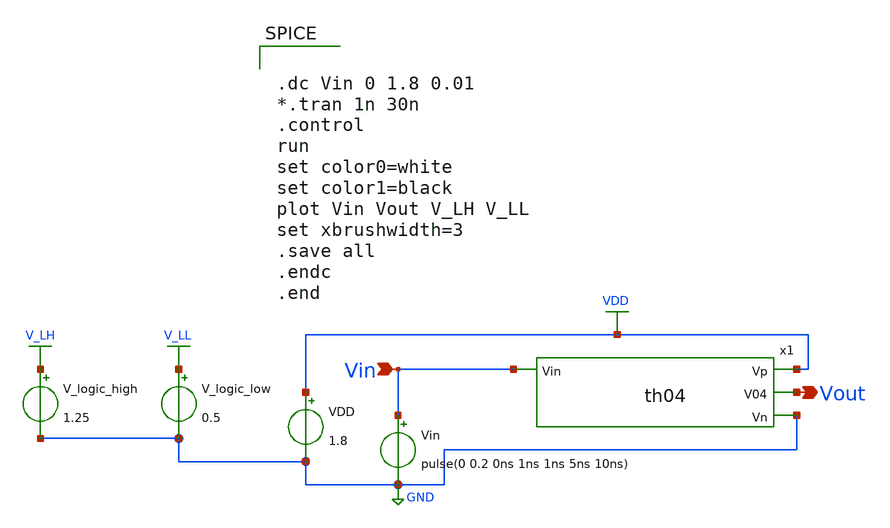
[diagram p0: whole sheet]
** sch_path: xschem/Vth_sch/Pre_layout/th04.sch
**.subckt th04 Vin Vout
*.ipin Vin
*.opin Vout
VDD VDD GND 1.8
Vin Vin GND pulse(0 0.2 0ns 1ns 1ns 5ns 10ns)
V_logic_high V_LH GND 1.25
V_logic_low V_LL GND 0.5
x1 VDD Vout Vin GND th04
**** begin user architecture code


.lib /usr/local/share/pdk/sky130A/libs.tech/ngspice/sky130.lib.spice tt

.save all





.dc Vin 0 1.8 0.01
*.tran 1n 30n
.control
run
set color0=white
set color1=black
plot Vin Vout V_LH V_LL
set xbrushwidth=3
.save all
.endc
.end


**** end user architecture code
**.ends

* expanding   symbol:  /home/exotic/Desktop/ASIC_ADC/xschem/Vth_sch/Symbol/th04.sym # of pins=4
** sym_path: xschem/Vth_sch/Symbol/th04.sym
** sch_path: xschem/Vth_sch/Symbol/th04.sch
.subckt th04 Vp V04 Vin Vn
*.opin Vn
*.opin Vp
*.ipin Vin
*.opin V04
XM3 V04 net1 Vp Vp sky130_fd_pr__pfet_01v8 L=0.220 W=0.42 nf=1 ad='int((nf+1)/2) * W/nf * 0.29' as='int((nf+2)/2) * W/nf * 0.29'
+ pd='2*int((nf+1)/2) * (W/nf + 0.29)' ps='2*int((nf+2)/2) * (W/nf + 0.29)' nrd='0.29 / W' nrs='0.29 / W'
+ sa=0 sb=0 sd=0 mult=1 m=1
XM4 V04 net1 Vn Vn sky130_fd_pr__nfet_01v8 L=0.193 W=0.36 nf=1 ad='int((nf+1)/2) * W/nf * 0.29' as='int((nf+2)/2) * W/nf * 0.29'
+ pd='2*int((nf+1)/2) * (W/nf + 0.29)' ps='2*int((nf+2)/2) * (W/nf + 0.29)' nrd='0.29 / W' nrs='0.29 / W'
+ sa=0 sb=0 sd=0 mult=1 m=1
XM1 net1 Vin net2 Vp sky130_fd_pr__pfet_01v8 L=0.193 W=0.42 nf=1 ad='int((nf+1)/2) * W/nf * 0.29' as='int((nf+2)/2) * W/nf * 0.29'
+ pd='2*int((nf+1)/2) * (W/nf + 0.29)' ps='2*int((nf+2)/2) * (W/nf + 0.29)' nrd='0.29 / W' nrs='0.29 / W'
+ sa=0 sb=0 sd=0 mult=1 m=1
XM0 net1 Vin Vn Vn sky130_fd_pr__nfet_01v8 L=0.220 W=0.36 nf=1 ad='int((nf+1)/2) * W/nf * 0.29' as='int((nf+2)/2) * W/nf * 0.29'
+ pd='2*int((nf+1)/2) * (W/nf + 0.29)' ps='2*int((nf+2)/2) * (W/nf + 0.29)' nrd='0.29 / W' nrs='0.29 / W'
+ sa=0 sb=0 sd=0 mult=1 m=1
XM2 Vp Vp net2 Vn sky130_fd_pr__nfet_01v8 L=0.151 W=0.36 nf=1 ad='int((nf+1)/2) * W/nf * 0.29' as='int((nf+2)/2) * W/nf * 0.29'
+ pd='2*int((nf+1)/2) * (W/nf + 0.29)' ps='2*int((nf+2)/2) * (W/nf + 0.29)' nrd='0.29 / W' nrs='0.29 / W'
+ sa=0 sb=0 sd=0 mult=1 m=1
.ends

.GLOBAL VDD
.GLOBAL GND
.GLOBAL V_LH
.GLOBAL V_LL
.end
